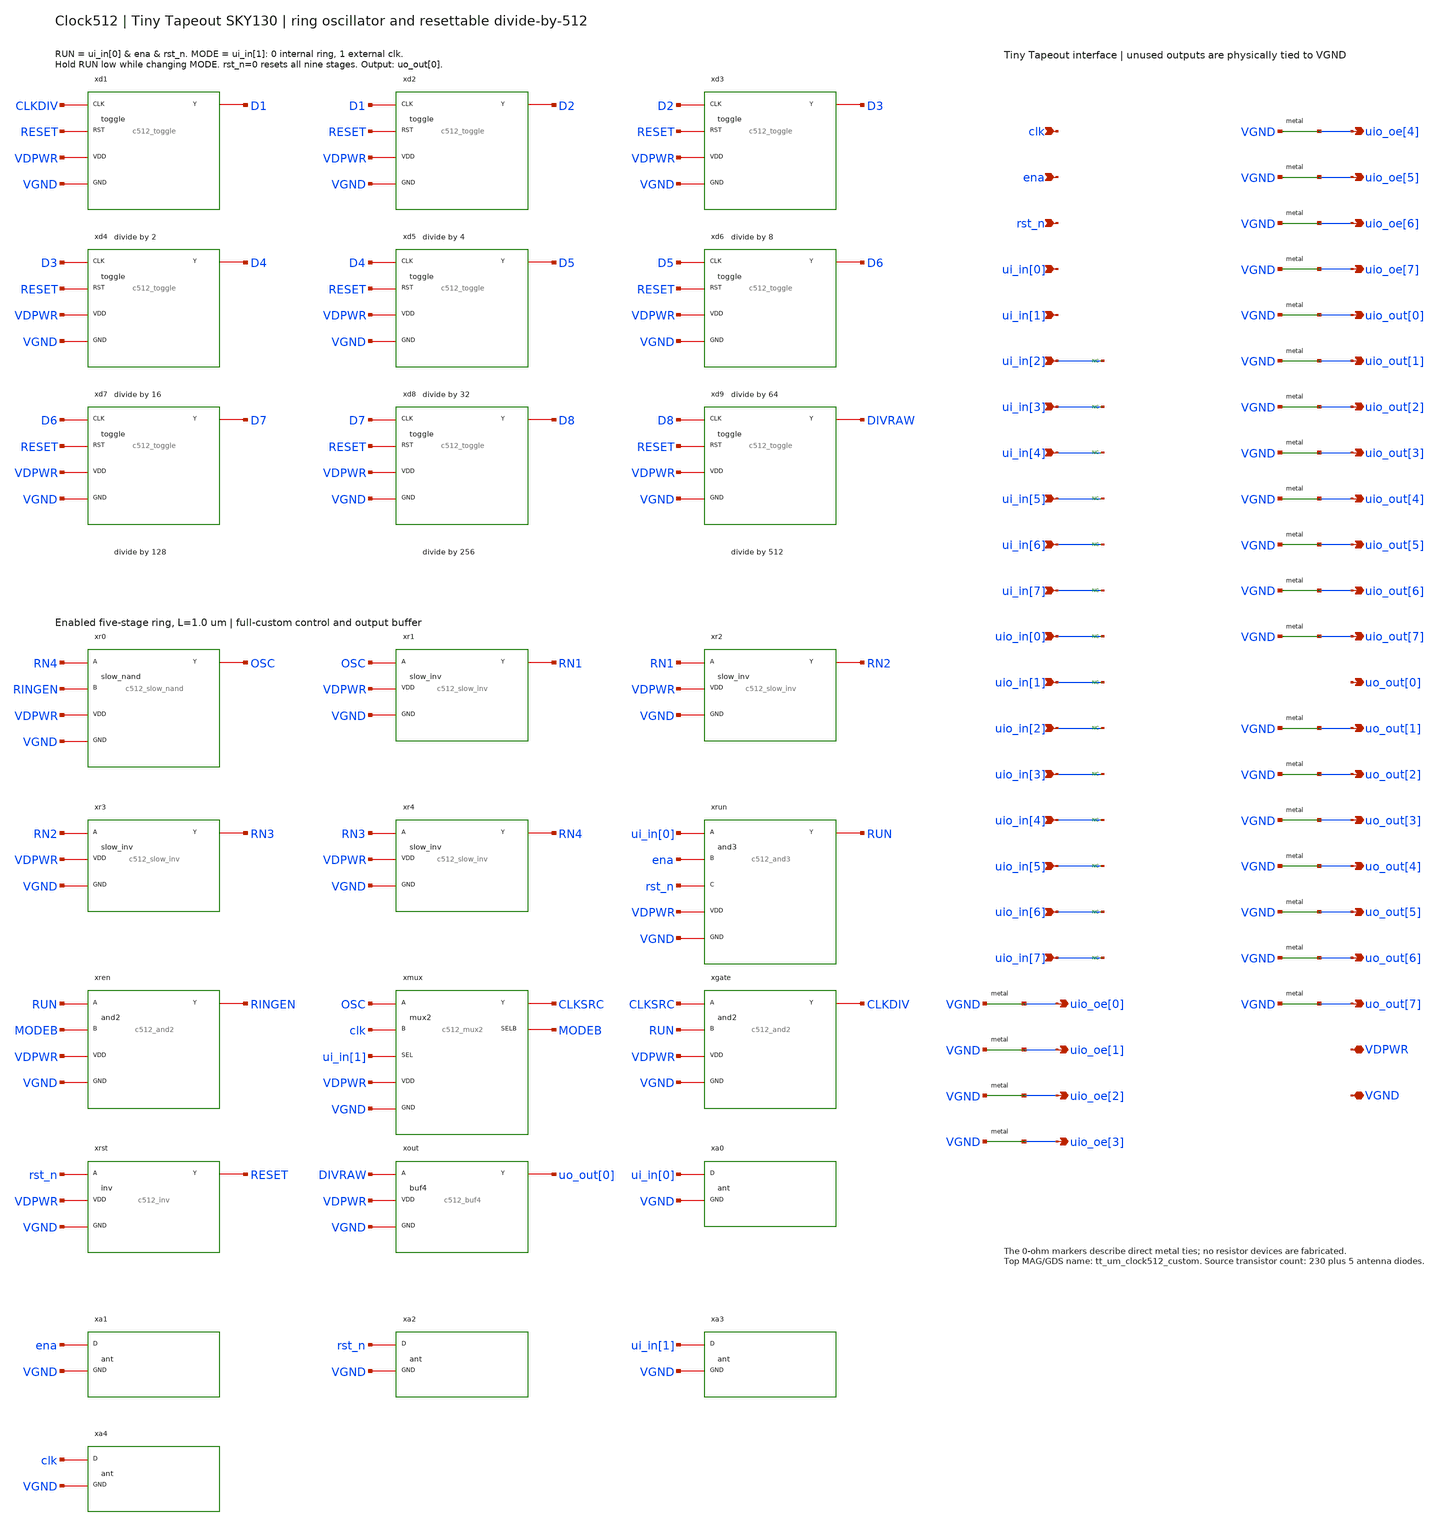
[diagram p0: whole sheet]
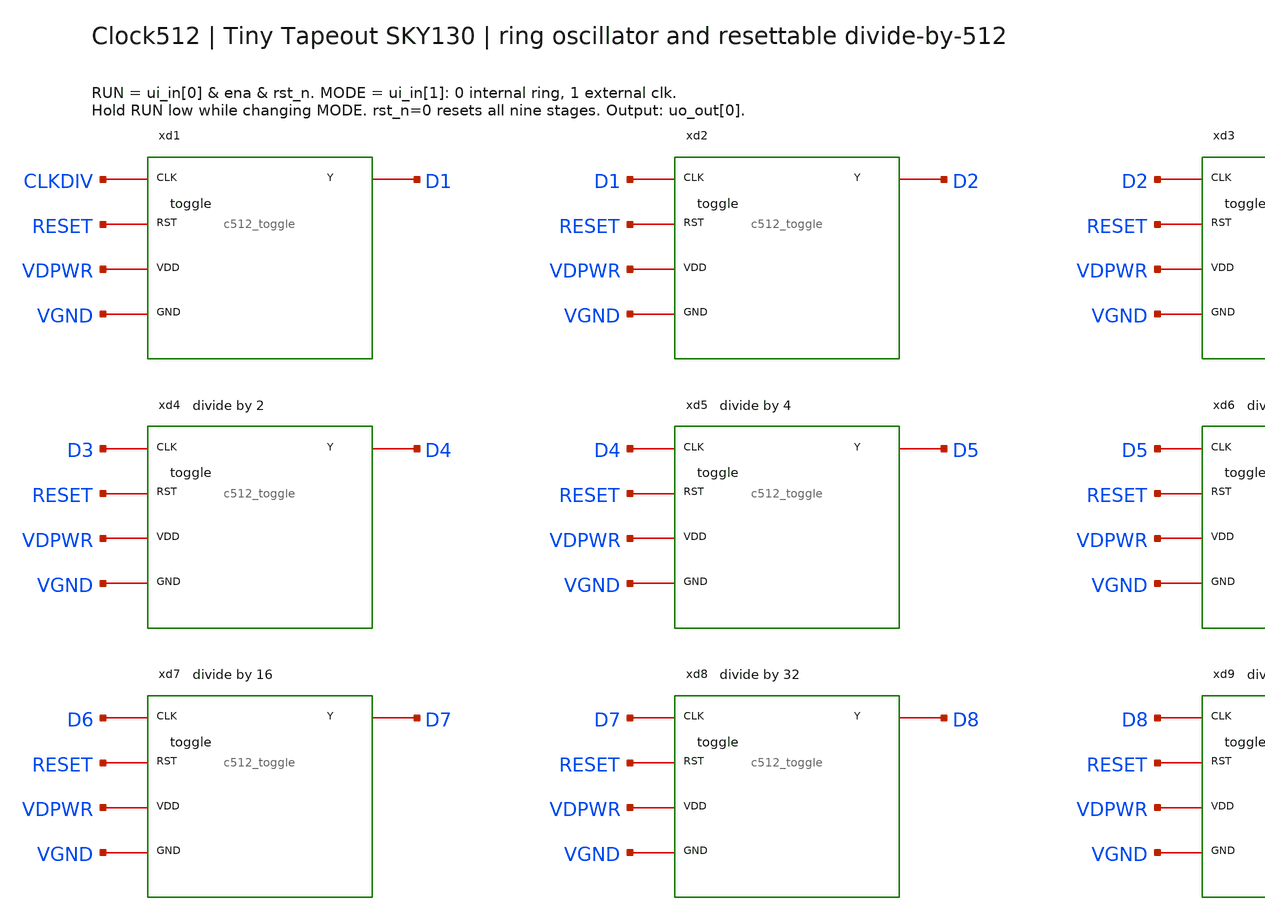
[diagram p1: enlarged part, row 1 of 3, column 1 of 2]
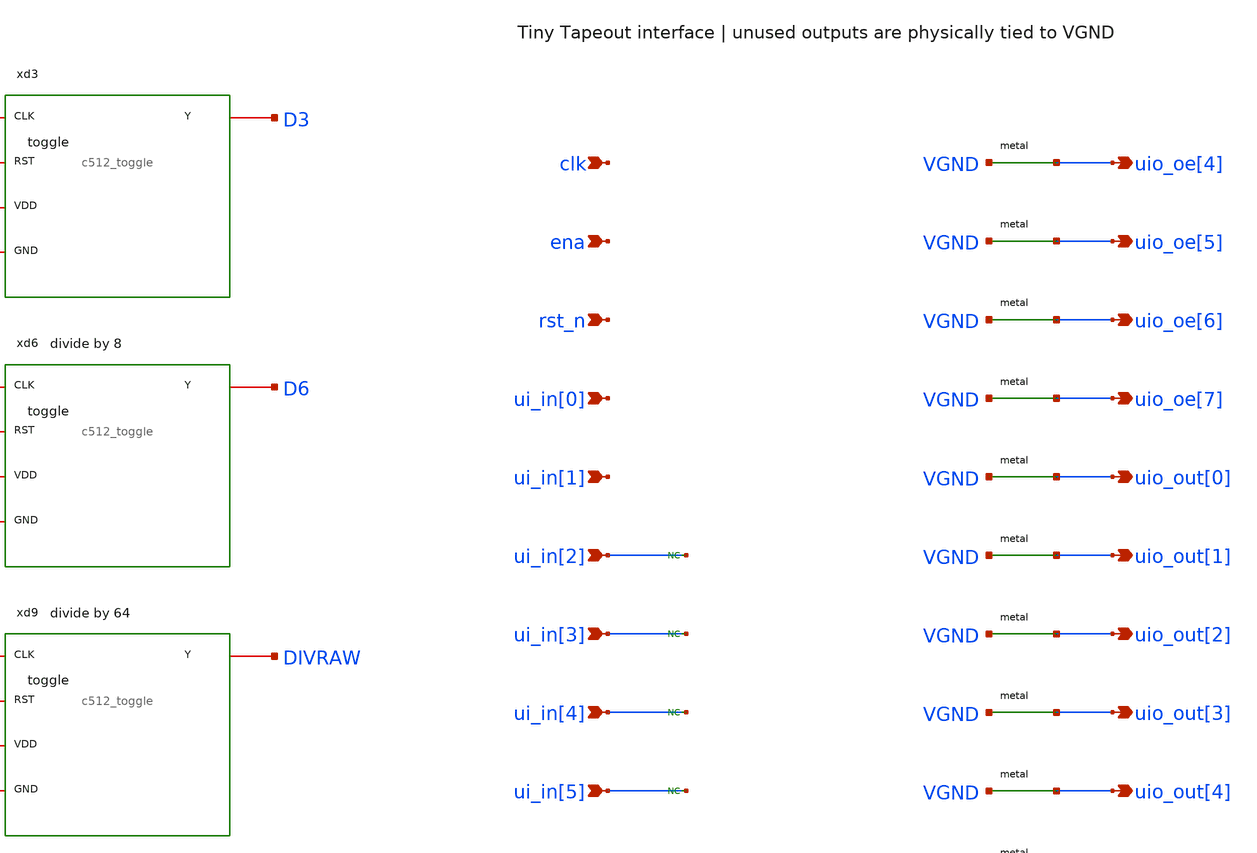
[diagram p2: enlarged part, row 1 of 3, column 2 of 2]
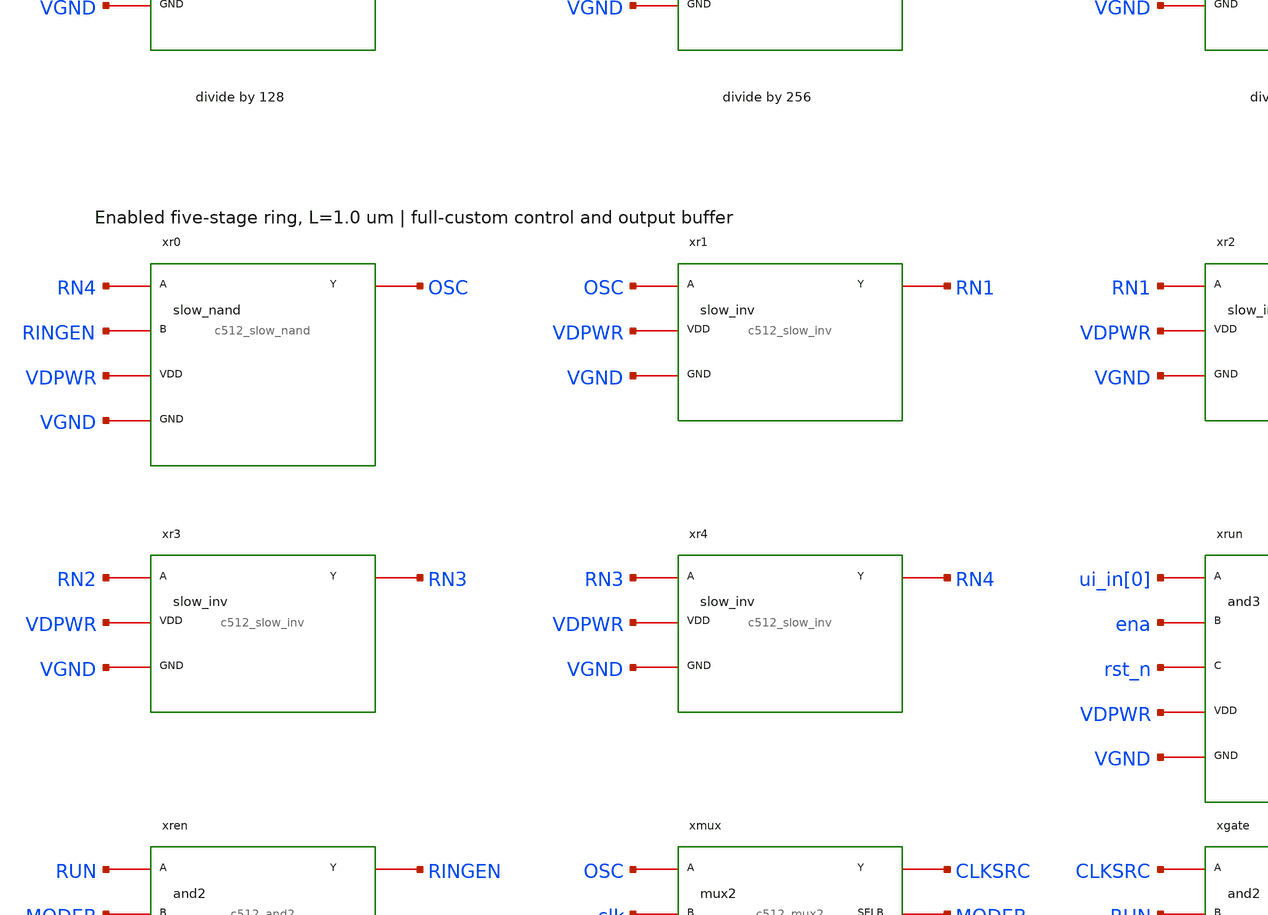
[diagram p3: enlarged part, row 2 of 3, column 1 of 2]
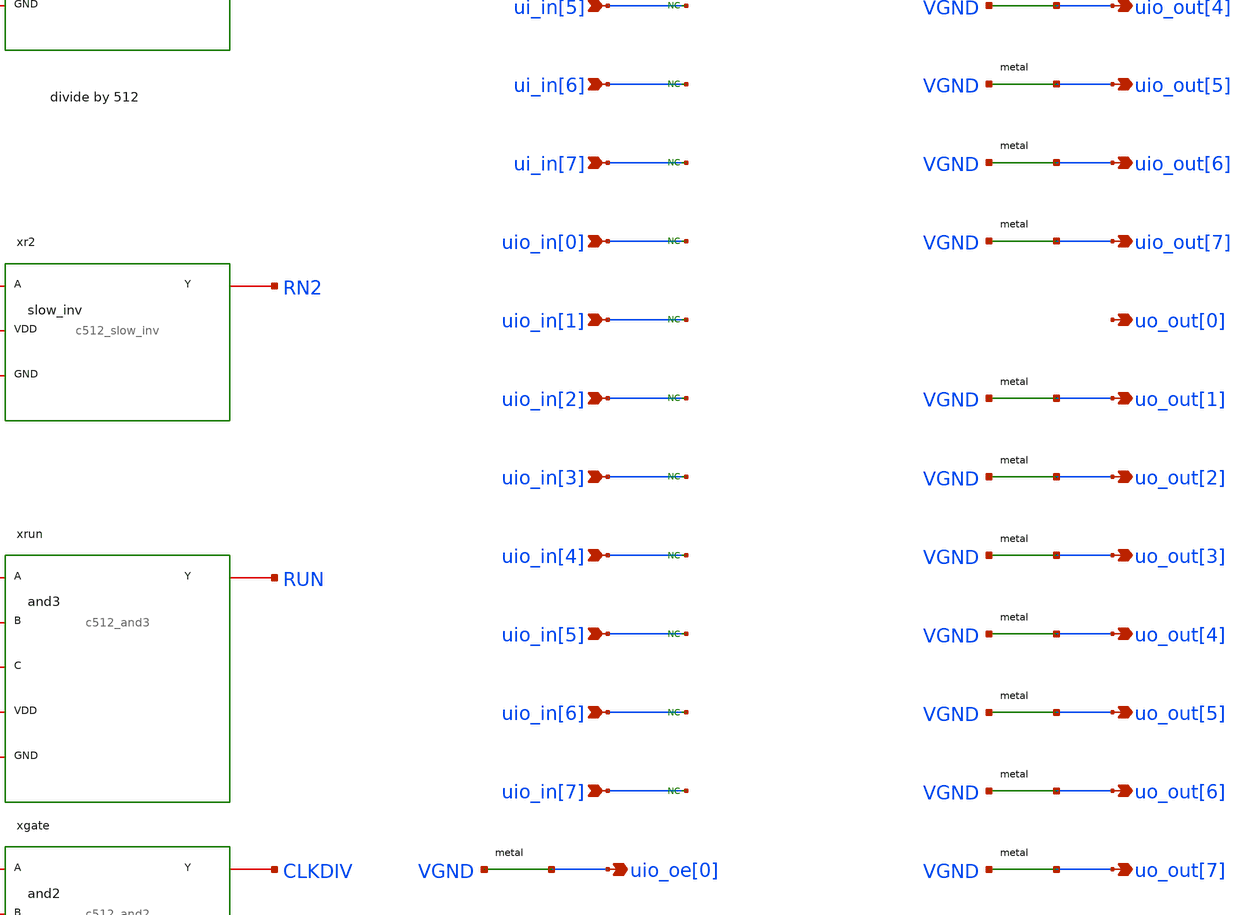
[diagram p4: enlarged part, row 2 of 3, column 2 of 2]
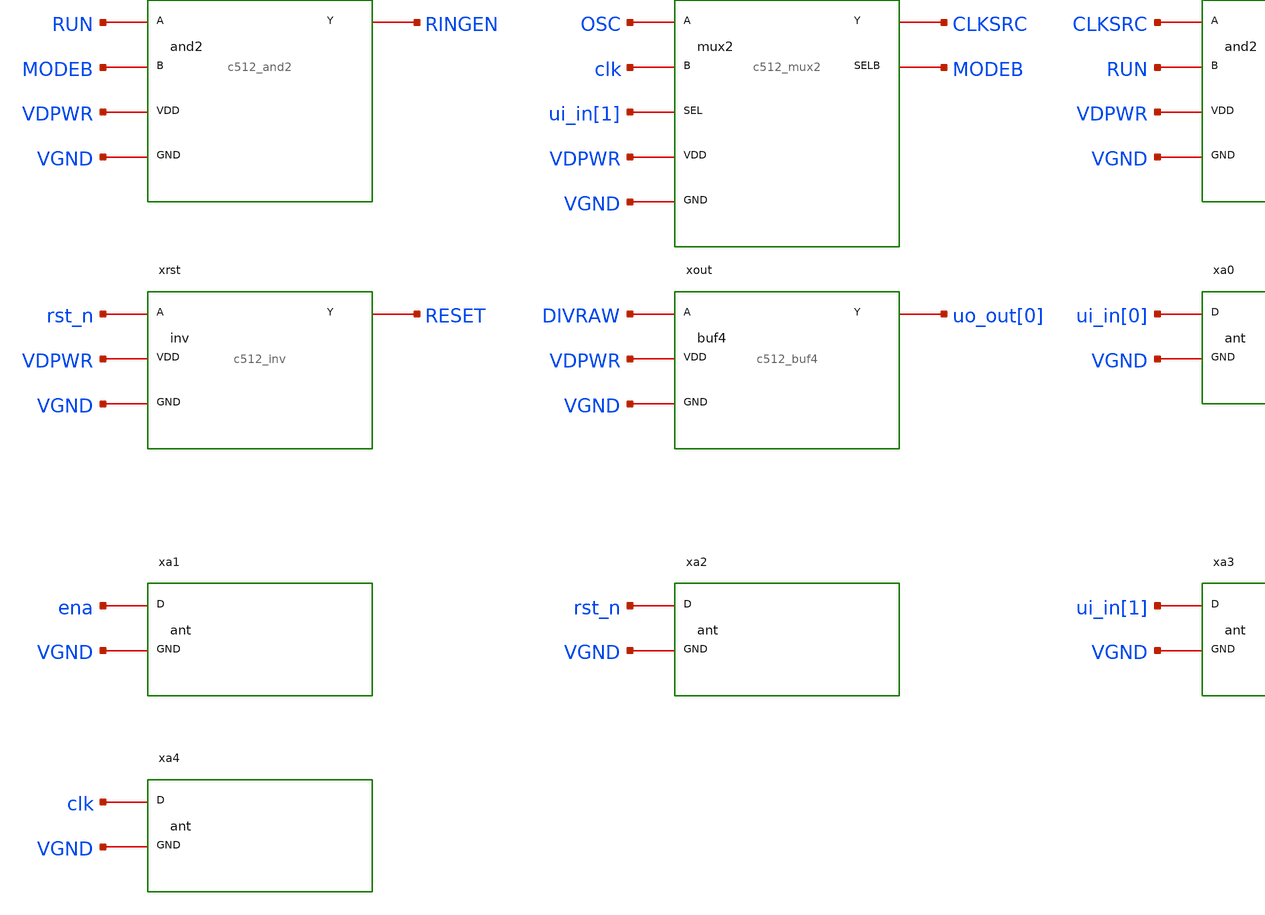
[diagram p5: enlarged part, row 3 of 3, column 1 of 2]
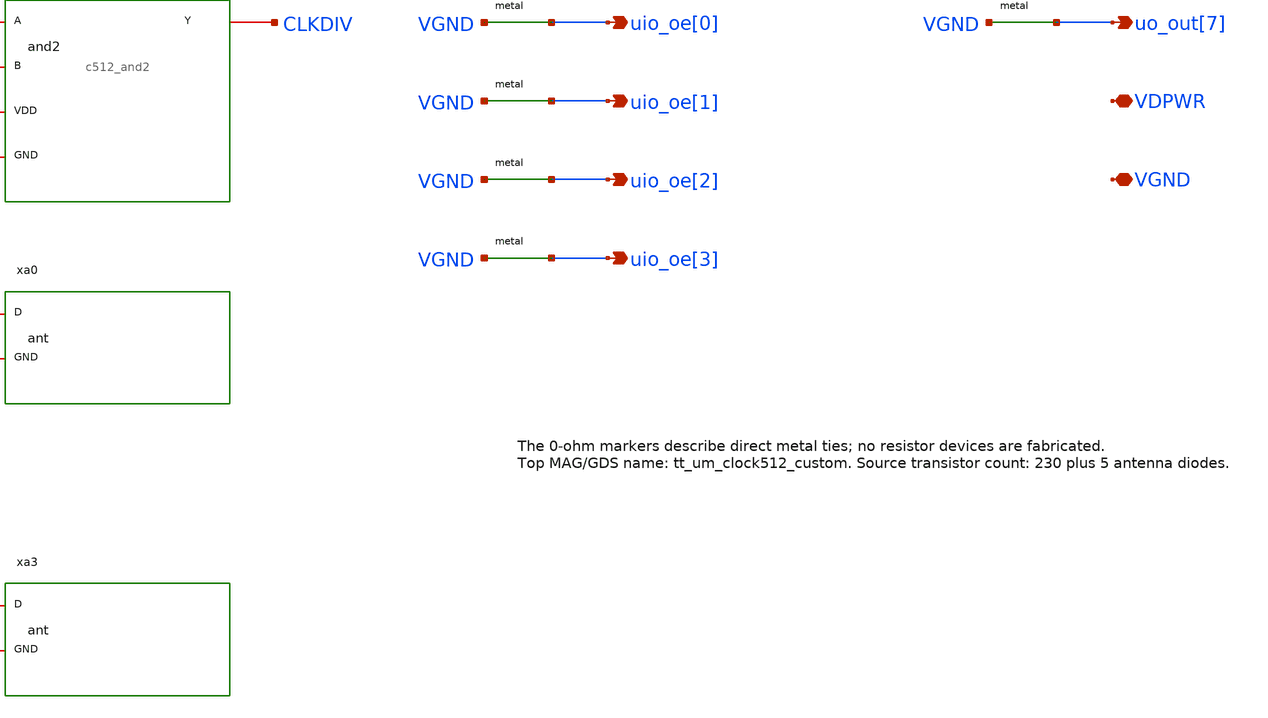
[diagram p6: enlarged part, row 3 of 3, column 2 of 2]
** sch_path: top.sch
**.subckt top clk ena rst_n ui_in[0] ui_in[1] ui_in[2] ui_in[3] ui_in[4] ui_in[5] ui_in[6] ui_in[7]
*+ uio_in[0] uio_in[1] uio_in[2] uio_in[3] uio_in[4] uio_in[5] uio_in[6] uio_in[7] uio_oe[0] uio_oe[1] uio_oe[2]
*+ uio_oe[3] uio_oe[4] uio_oe[5] uio_oe[6] uio_oe[7] uio_out[0] uio_out[1] uio_out[2] uio_out[3] uio_out[4]
*+ uio_out[5] uio_out[6] uio_out[7] uo_out[0] uo_out[1] uo_out[2] uo_out[3] uo_out[4] uo_out[5] uo_out[6]
*+ uo_out[7] VDPWR VGND
*.ipin clk
*.ipin ena
*.ipin rst_n
*.ipin ui_in[0]
*.ipin ui_in[1]
*.ipin ui_in[2]
*.ipin ui_in[3]
*.ipin ui_in[4]
*.ipin ui_in[5]
*.ipin ui_in[6]
*.ipin ui_in[7]
*.ipin uio_in[0]
*.ipin uio_in[1]
*.ipin uio_in[2]
*.ipin uio_in[3]
*.ipin uio_in[4]
*.ipin uio_in[5]
*.ipin uio_in[6]
*.ipin uio_in[7]
*.opin uio_oe[0]
*.opin uio_oe[1]
*.opin uio_oe[2]
*.opin uio_oe[3]
*.opin uio_oe[4]
*.opin uio_oe[5]
*.opin uio_oe[6]
*.opin uio_oe[7]
*.opin uio_out[0]
*.opin uio_out[1]
*.opin uio_out[2]
*.opin uio_out[3]
*.opin uio_out[4]
*.opin uio_out[5]
*.opin uio_out[6]
*.opin uio_out[7]
*.opin uo_out[0]
*.opin uo_out[1]
*.opin uo_out[2]
*.opin uo_out[3]
*.opin uo_out[4]
*.opin uo_out[5]
*.opin uo_out[6]
*.opin uo_out[7]
*.iopin VDPWR
*.iopin VGND
xd1 D1 CLKDIV RESET VDPWR VGND c512_toggle
xd2 D2 D1 RESET VDPWR VGND c512_toggle
xd3 D3 D2 RESET VDPWR VGND c512_toggle
xd4 D4 D3 RESET VDPWR VGND c512_toggle
xd5 D5 D4 RESET VDPWR VGND c512_toggle
xd6 D6 D5 RESET VDPWR VGND c512_toggle
xd7 D7 D6 RESET VDPWR VGND c512_toggle
xd8 D8 D7 RESET VDPWR VGND c512_toggle
xd9 DIVRAW D8 RESET VDPWR VGND c512_toggle
xr0 OSC RN4 RINGEN VDPWR VGND c512_slow_nand
xr1 RN1 OSC VDPWR VGND c512_slow_inv
xr2 RN2 RN1 VDPWR VGND c512_slow_inv
xr3 RN3 RN2 VDPWR VGND c512_slow_inv
xr4 RN4 RN3 VDPWR VGND c512_slow_inv
xrun RUN ui_in[0] ena rst_n VDPWR VGND c512_and3
xren RINGEN RUN MODEB VDPWR VGND c512_and2
xmux CLKSRC OSC clk ui_in[1] MODEB VDPWR VGND c512_mux2
xgate CLKDIV CLKSRC RUN VDPWR VGND c512_and2
xrst RESET rst_n VDPWR VGND c512_inv
xout uo_out[0] DIVRAW VDPWR VGND c512_buf4
xa0 ui_in[0] VGND c512_ant
xa1 ena VGND c512_ant
xa2 rst_n VGND c512_ant
xa3 ui_in[1] VGND c512_ant
xa4 clk VGND c512_ant
* noconn ui_in[2]
* noconn ui_in[3]
* noconn ui_in[4]
* noconn ui_in[5]
* noconn ui_in[6]
* noconn ui_in[7]
* noconn uio_in[0]
* noconn uio_in[1]
* noconn uio_in[2]
* noconn uio_in[3]
* noconn uio_in[4]
* noconn uio_in[5]
* noconn uio_in[6]
* noconn uio_in[7]
Rtie19 VGND uio_oe[0] 0
Rtie20 VGND uio_oe[1] 0
Rtie21 VGND uio_oe[2] 0
Rtie22 VGND uio_oe[3] 0
Rtie23 VGND uio_oe[4] 0
Rtie24 VGND uio_oe[5] 0
Rtie25 VGND uio_oe[6] 0
Rtie26 VGND uio_oe[7] 0
Rtie27 VGND uio_out[0] 0
Rtie28 VGND uio_out[1] 0
Rtie29 VGND uio_out[2] 0
Rtie30 VGND uio_out[3] 0
Rtie31 VGND uio_out[4] 0
Rtie32 VGND uio_out[5] 0
Rtie33 VGND uio_out[6] 0
Rtie34 VGND uio_out[7] 0
Rtie36 VGND uo_out[1] 0
Rtie37 VGND uo_out[2] 0
Rtie38 VGND uo_out[3] 0
Rtie39 VGND uo_out[4] 0
Rtie40 VGND uo_out[5] 0
Rtie41 VGND uo_out[6] 0
Rtie42 VGND uo_out[7] 0
**.ends

* expanding   symbol:  c512_toggle.sym # of pins=5
** sym_path: c512_toggle.sym
** sch_path: c512_toggle.sch
.subckt c512_toggle Y CLK RST VDD GND
*.opin Y
*.ipin CLK
*.ipin RST
*.iopin VDD
*.iopin GND
XM1 CLKB CLK GND GND sky130_fd_pr__nfet_01v8 L=0.15 W=1 nf=1 ad=0.29 as=0.29 pd=2.58 ps=2.58
+ nrd=0.29 nrs=0.29 sa=0 sb=0 sd=0 mult=1 m=1
XM2 CLKB CLK VDD VDD sky130_fd_pr__pfet_01v8 L=0.15 W=2 nf=1 ad=0.58 as=0.58 pd=4.58 ps=4.58
+ nrd=0.145 nrs=0.145 sa=0 sb=0 sd=0 mult=1 m=1
XM3 M CLKB QB GND sky130_fd_pr__nfet_01v8 L=0.15 W=1 nf=1 ad=0.29 as=0.29 pd=2.58 ps=2.58 nrd=0.29
+ nrs=0.29 sa=0 sb=0 sd=0 mult=1 m=1
XM4 M CLK QB VDD sky130_fd_pr__pfet_01v8 L=0.15 W=2 nf=1 ad=0.58 as=0.58 pd=4.58 ps=4.58 nrd=0.145
+ nrs=0.145 sa=0 sb=0 sd=0 mult=1 m=1
XM5 MB M GND GND sky130_fd_pr__nfet_01v8 L=0.15 W=1 nf=1 ad=0.29 as=0.29 pd=2.58 ps=2.58 nrd=0.29
+ nrs=0.29 sa=0 sb=0 sd=0 mult=1 m=1
XM6 MB M VDD VDD sky130_fd_pr__pfet_01v8 L=0.15 W=2 nf=1 ad=0.58 as=0.58 pd=4.58 ps=4.58 nrd=0.145
+ nrs=0.145 sa=0 sb=0 sd=0 mult=1 m=1
XM7 MF MB GND GND sky130_fd_pr__nfet_01v8 L=0.15 W=1 nf=1 ad=0.29 as=0.29 pd=2.58 ps=2.58 nrd=0.29
+ nrs=0.29 sa=0 sb=0 sd=0 mult=1 m=1
XM8 MF MB VDD VDD sky130_fd_pr__pfet_01v8 L=0.15 W=2 nf=1 ad=0.58 as=0.58 pd=4.58 ps=4.58 nrd=0.145
+ nrs=0.145 sa=0 sb=0 sd=0 mult=1 m=1
XM9 M CLK MF GND sky130_fd_pr__nfet_01v8 L=0.15 W=1 nf=1 ad=0.29 as=0.29 pd=2.58 ps=2.58 nrd=0.29
+ nrs=0.29 sa=0 sb=0 sd=0 mult=1 m=1
XM10 M CLKB MF VDD sky130_fd_pr__pfet_01v8 L=0.15 W=2 nf=1 ad=0.58 as=0.58 pd=4.58 ps=4.58 nrd=0.145
+ nrs=0.145 sa=0 sb=0 sd=0 mult=1 m=1
XM11 S CLK MB GND sky130_fd_pr__nfet_01v8 L=0.15 W=1 nf=1 ad=0.29 as=0.29 pd=2.58 ps=2.58 nrd=0.29
+ nrs=0.29 sa=0 sb=0 sd=0 mult=1 m=1
XM12 S CLKB MB VDD sky130_fd_pr__pfet_01v8 L=0.15 W=2 nf=1 ad=0.58 as=0.58 pd=4.58 ps=4.58 nrd=0.145
+ nrs=0.145 sa=0 sb=0 sd=0 mult=1 m=1
XM13 Y S GND GND sky130_fd_pr__nfet_01v8 L=0.15 W=1 nf=1 ad=0.29 as=0.29 pd=2.58 ps=2.58 nrd=0.29
+ nrs=0.29 sa=0 sb=0 sd=0 mult=1 m=1
XM14 Y RST GND GND sky130_fd_pr__nfet_01v8 L=0.15 W=1 nf=1 ad=0.29 as=0.29 pd=2.58 ps=2.58 nrd=0.29
+ nrs=0.29 sa=0 sb=0 sd=0 mult=1 m=1
XM15 PZ S VDD VDD sky130_fd_pr__pfet_01v8 L=0.15 W=2 nf=1 ad=0.58 as=0.58 pd=4.58 ps=4.58 nrd=0.145
+ nrs=0.145 sa=0 sb=0 sd=0 mult=1 m=1
XM16 Y RST PZ VDD sky130_fd_pr__pfet_01v8 L=0.15 W=2 nf=1 ad=0.58 as=0.58 pd=4.58 ps=4.58 nrd=0.145
+ nrs=0.145 sa=0 sb=0 sd=0 mult=1 m=1
XM17 QB Y GND GND sky130_fd_pr__nfet_01v8 L=0.15 W=1 nf=1 ad=0.29 as=0.29 pd=2.58 ps=2.58 nrd=0.29
+ nrs=0.29 sa=0 sb=0 sd=0 mult=1 m=1
XM18 QB Y VDD VDD sky130_fd_pr__pfet_01v8 L=0.15 W=2 nf=1 ad=0.58 as=0.58 pd=4.58 ps=4.58 nrd=0.145
+ nrs=0.145 sa=0 sb=0 sd=0 mult=1 m=1
XM19 S CLKB QB GND sky130_fd_pr__nfet_01v8 L=0.15 W=1 nf=1 ad=0.29 as=0.29 pd=2.58 ps=2.58 nrd=0.29
+ nrs=0.29 sa=0 sb=0 sd=0 mult=1 m=1
XM20 S CLK QB VDD sky130_fd_pr__pfet_01v8 L=0.15 W=2 nf=1 ad=0.58 as=0.58 pd=4.58 ps=4.58 nrd=0.145
+ nrs=0.145 sa=0 sb=0 sd=0 mult=1 m=1
.ends


* expanding   symbol:  c512_slow_nand.sym # of pins=5
** sym_path: c512_slow_nand.sym
** sch_path: c512_slow_nand.sch
.subckt c512_slow_nand Y A B VDD GND
*.opin Y
*.ipin A
*.ipin B
*.iopin VDD
*.iopin GND
XM1 Y A VDD VDD sky130_fd_pr__pfet_01v8 L=1.0 W=2 nf=1 ad=0.58 as=0.58 pd=4.58 ps=4.58 nrd=0.145
+ nrs=0.145 sa=0 sb=0 sd=0 mult=1 m=1
XM2 Y B VDD VDD sky130_fd_pr__pfet_01v8 L=1.0 W=2 nf=1 ad=0.58 as=0.58 pd=4.58 ps=4.58 nrd=0.145
+ nrs=0.145 sa=0 sb=0 sd=0 mult=1 m=1
XM3 Y A z1 GND sky130_fd_pr__nfet_01v8 L=1.0 W=1 nf=1 ad=0.29 as=0.29 pd=2.58 ps=2.58 nrd=0.29
+ nrs=0.29 sa=0 sb=0 sd=0 mult=1 m=1
XM4 z1 B GND GND sky130_fd_pr__nfet_01v8 L=1.0 W=1 nf=1 ad=0.29 as=0.29 pd=2.58 ps=2.58 nrd=0.29
+ nrs=0.29 sa=0 sb=0 sd=0 mult=1 m=1
.ends


* expanding   symbol:  c512_slow_inv.sym # of pins=4
** sym_path: c512_slow_inv.sym
** sch_path: c512_slow_inv.sch
.subckt c512_slow_inv Y A VDD GND
*.opin Y
*.ipin A
*.iopin VDD
*.iopin GND
XM1 Y A GND GND sky130_fd_pr__nfet_01v8 L=1.0 W=1 nf=1 ad=0.29 as=0.29 pd=2.58 ps=2.58 nrd=0.29
+ nrs=0.29 sa=0 sb=0 sd=0 mult=1 m=1
XM2 Y A VDD VDD sky130_fd_pr__pfet_01v8 L=1.0 W=2 nf=1 ad=0.58 as=0.58 pd=4.58 ps=4.58 nrd=0.145
+ nrs=0.145 sa=0 sb=0 sd=0 mult=1 m=1
.ends


* expanding   symbol:  c512_and3.sym # of pins=6
** sym_path: c512_and3.sym
** sch_path: c512_and3.sch
.subckt c512_and3 Y A B C VDD GND
*.opin Y
*.ipin A
*.ipin B
*.ipin C
*.iopin VDD
*.iopin GND
XM1 ZN A VDD VDD sky130_fd_pr__pfet_01v8 L=0.15 W=2 nf=1 ad=0.58 as=0.58 pd=4.58 ps=4.58 nrd=0.145
+ nrs=0.145 sa=0 sb=0 sd=0 mult=1 m=1
XM2 ZN B VDD VDD sky130_fd_pr__pfet_01v8 L=0.15 W=2 nf=1 ad=0.58 as=0.58 pd=4.58 ps=4.58 nrd=0.145
+ nrs=0.145 sa=0 sb=0 sd=0 mult=1 m=1
XM3 ZN C VDD VDD sky130_fd_pr__pfet_01v8 L=0.15 W=2 nf=1 ad=0.58 as=0.58 pd=4.58 ps=4.58 nrd=0.145
+ nrs=0.145 sa=0 sb=0 sd=0 mult=1 m=1
XM4 ZN A z1 GND sky130_fd_pr__nfet_01v8 L=0.15 W=1 nf=1 ad=0.29 as=0.29 pd=2.58 ps=2.58 nrd=0.29
+ nrs=0.29 sa=0 sb=0 sd=0 mult=1 m=1
XM5 z1 B z2 GND sky130_fd_pr__nfet_01v8 L=0.15 W=1 nf=1 ad=0.29 as=0.29 pd=2.58 ps=2.58 nrd=0.29
+ nrs=0.29 sa=0 sb=0 sd=0 mult=1 m=1
XM6 z2 C GND GND sky130_fd_pr__nfet_01v8 L=0.15 W=1 nf=1 ad=0.29 as=0.29 pd=2.58 ps=2.58 nrd=0.29
+ nrs=0.29 sa=0 sb=0 sd=0 mult=1 m=1
XM7 Y ZN GND GND sky130_fd_pr__nfet_01v8 L=0.15 W=1 nf=1 ad=0.29 as=0.29 pd=2.58 ps=2.58 nrd=0.29
+ nrs=0.29 sa=0 sb=0 sd=0 mult=1 m=1
XM8 Y ZN VDD VDD sky130_fd_pr__pfet_01v8 L=0.15 W=2 nf=1 ad=0.58 as=0.58 pd=4.58 ps=4.58 nrd=0.145
+ nrs=0.145 sa=0 sb=0 sd=0 mult=1 m=1
.ends


* expanding   symbol:  c512_and2.sym # of pins=5
** sym_path: c512_and2.sym
** sch_path: c512_and2.sch
.subckt c512_and2 Y A B VDD GND
*.opin Y
*.ipin A
*.ipin B
*.iopin VDD
*.iopin GND
XM1 ZN A VDD VDD sky130_fd_pr__pfet_01v8 L=0.15 W=2 nf=1 ad=0.58 as=0.58 pd=4.58 ps=4.58 nrd=0.145
+ nrs=0.145 sa=0 sb=0 sd=0 mult=1 m=1
XM2 ZN B VDD VDD sky130_fd_pr__pfet_01v8 L=0.15 W=2 nf=1 ad=0.58 as=0.58 pd=4.58 ps=4.58 nrd=0.145
+ nrs=0.145 sa=0 sb=0 sd=0 mult=1 m=1
XM3 ZN A z1 GND sky130_fd_pr__nfet_01v8 L=0.15 W=1 nf=1 ad=0.29 as=0.29 pd=2.58 ps=2.58 nrd=0.29
+ nrs=0.29 sa=0 sb=0 sd=0 mult=1 m=1
XM4 z1 B GND GND sky130_fd_pr__nfet_01v8 L=0.15 W=1 nf=1 ad=0.29 as=0.29 pd=2.58 ps=2.58 nrd=0.29
+ nrs=0.29 sa=0 sb=0 sd=0 mult=1 m=1
XM5 Y ZN GND GND sky130_fd_pr__nfet_01v8 L=0.15 W=1 nf=1 ad=0.29 as=0.29 pd=2.58 ps=2.58 nrd=0.29
+ nrs=0.29 sa=0 sb=0 sd=0 mult=1 m=1
XM6 Y ZN VDD VDD sky130_fd_pr__pfet_01v8 L=0.15 W=2 nf=1 ad=0.58 as=0.58 pd=4.58 ps=4.58 nrd=0.145
+ nrs=0.145 sa=0 sb=0 sd=0 mult=1 m=1
.ends


* expanding   symbol:  c512_mux2.sym # of pins=7
** sym_path: c512_mux2.sym
** sch_path: c512_mux2.sch
.subckt c512_mux2 Y A B SEL SELB VDD GND
*.opin Y
*.ipin A
*.ipin B
*.ipin SEL
*.opin SELB
*.iopin VDD
*.iopin GND
XM1 SELB SEL GND GND sky130_fd_pr__nfet_01v8 L=0.15 W=1 nf=1 ad=0.29 as=0.29 pd=2.58 ps=2.58
+ nrd=0.29 nrs=0.29 sa=0 sb=0 sd=0 mult=1 m=1
XM2 SELB SEL VDD VDD sky130_fd_pr__pfet_01v8 L=0.15 W=2 nf=1 ad=0.58 as=0.58 pd=4.58 ps=4.58
+ nrd=0.145 nrs=0.145 sa=0 sb=0 sd=0 mult=1 m=1
XM3 Y SELB A GND sky130_fd_pr__nfet_01v8 L=0.15 W=1 nf=1 ad=0.29 as=0.29 pd=2.58 ps=2.58 nrd=0.29
+ nrs=0.29 sa=0 sb=0 sd=0 mult=1 m=1
XM4 Y SEL A VDD sky130_fd_pr__pfet_01v8 L=0.15 W=2 nf=1 ad=0.58 as=0.58 pd=4.58 ps=4.58 nrd=0.145
+ nrs=0.145 sa=0 sb=0 sd=0 mult=1 m=1
XM5 Y SEL B GND sky130_fd_pr__nfet_01v8 L=0.15 W=1 nf=1 ad=0.29 as=0.29 pd=2.58 ps=2.58 nrd=0.29
+ nrs=0.29 sa=0 sb=0 sd=0 mult=1 m=1
XM6 Y SELB B VDD sky130_fd_pr__pfet_01v8 L=0.15 W=2 nf=1 ad=0.58 as=0.58 pd=4.58 ps=4.58 nrd=0.145
+ nrs=0.145 sa=0 sb=0 sd=0 mult=1 m=1
.ends


* expanding   symbol:  c512_inv.sym # of pins=4
** sym_path: c512_inv.sym
** sch_path: c512_inv.sch
.subckt c512_inv Y A VDD GND
*.opin Y
*.ipin A
*.iopin VDD
*.iopin GND
XM1 Y A GND GND sky130_fd_pr__nfet_01v8 L=0.15 W=1 nf=1 ad=0.29 as=0.29 pd=2.58 ps=2.58 nrd=0.29
+ nrs=0.29 sa=0 sb=0 sd=0 mult=1 m=1
XM2 Y A VDD VDD sky130_fd_pr__pfet_01v8 L=0.15 W=2 nf=1 ad=0.58 as=0.58 pd=4.58 ps=4.58 nrd=0.145
+ nrs=0.145 sa=0 sb=0 sd=0 mult=1 m=1
.ends


* expanding   symbol:  c512_buf4.sym # of pins=4
** sym_path: c512_buf4.sym
** sch_path: c512_buf4.sch
.subckt c512_buf4 Y A VDD GND
*.opin Y
*.ipin A
*.iopin VDD
*.iopin GND
XM1 Z A GND GND sky130_fd_pr__nfet_01v8 L=0.15 W=1 nf=1 ad=0.29 as=0.29 pd=2.58 ps=2.58 nrd=0.29
+ nrs=0.29 sa=0 sb=0 sd=0 mult=1 m=1
XM2 Z A VDD VDD sky130_fd_pr__pfet_01v8 L=0.15 W=2 nf=1 ad=0.58 as=0.58 pd=4.58 ps=4.58 nrd=0.145
+ nrs=0.145 sa=0 sb=0 sd=0 mult=1 m=1
XM3 Y Z GND GND sky130_fd_pr__nfet_01v8 L=0.15 W=1 nf=1 ad=0.29 as=0.29 pd=2.58 ps=2.58 nrd=0.29
+ nrs=0.29 sa=0 sb=0 sd=0 mult=1 m=1
XM4 Y Z VDD VDD sky130_fd_pr__pfet_01v8 L=0.15 W=2 nf=1 ad=0.58 as=0.58 pd=4.58 ps=4.58 nrd=0.145
+ nrs=0.145 sa=0 sb=0 sd=0 mult=1 m=1
XM5 Y Z GND GND sky130_fd_pr__nfet_01v8 L=0.15 W=1 nf=1 ad=0.29 as=0.29 pd=2.58 ps=2.58 nrd=0.29
+ nrs=0.29 sa=0 sb=0 sd=0 mult=1 m=1
XM6 Y Z VDD VDD sky130_fd_pr__pfet_01v8 L=0.15 W=2 nf=1 ad=0.58 as=0.58 pd=4.58 ps=4.58 nrd=0.145
+ nrs=0.145 sa=0 sb=0 sd=0 mult=1 m=1
XM7 Y Z GND GND sky130_fd_pr__nfet_01v8 L=0.15 W=1 nf=1 ad=0.29 as=0.29 pd=2.58 ps=2.58 nrd=0.29
+ nrs=0.29 sa=0 sb=0 sd=0 mult=1 m=1
XM8 Y Z VDD VDD sky130_fd_pr__pfet_01v8 L=0.15 W=2 nf=1 ad=0.58 as=0.58 pd=4.58 ps=4.58 nrd=0.145
+ nrs=0.145 sa=0 sb=0 sd=0 mult=1 m=1
XM9 Y Z GND GND sky130_fd_pr__nfet_01v8 L=0.15 W=1 nf=1 ad=0.29 as=0.29 pd=2.58 ps=2.58 nrd=0.29
+ nrs=0.29 sa=0 sb=0 sd=0 mult=1 m=1
XM10 Y Z VDD VDD sky130_fd_pr__pfet_01v8 L=0.15 W=2 nf=1 ad=0.58 as=0.58 pd=4.58 ps=4.58 nrd=0.145
+ nrs=0.145 sa=0 sb=0 sd=0 mult=1 m=1
.ends


* expanding   symbol:  c512_ant.sym # of pins=2
** sym_path: c512_ant.sym
** sch_path: c512_ant.sch
.subckt c512_ant D GND
*.iopin D
*.iopin GND
XD1 GND D sky130_fd_pr__diode_pw2nd_05v5 area=2.25 pj=4e6
.ends

.end
